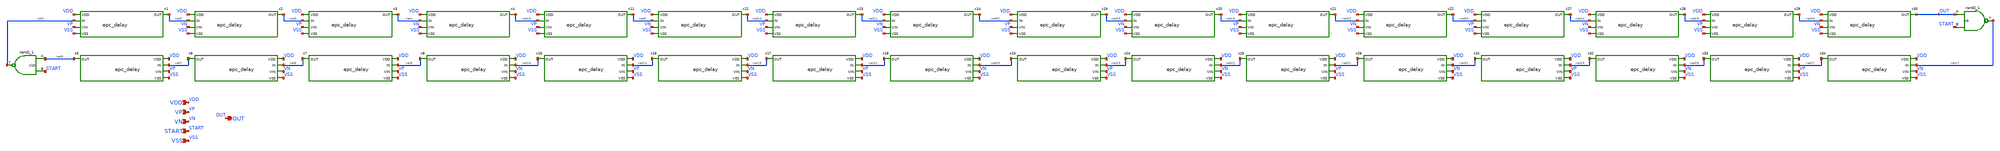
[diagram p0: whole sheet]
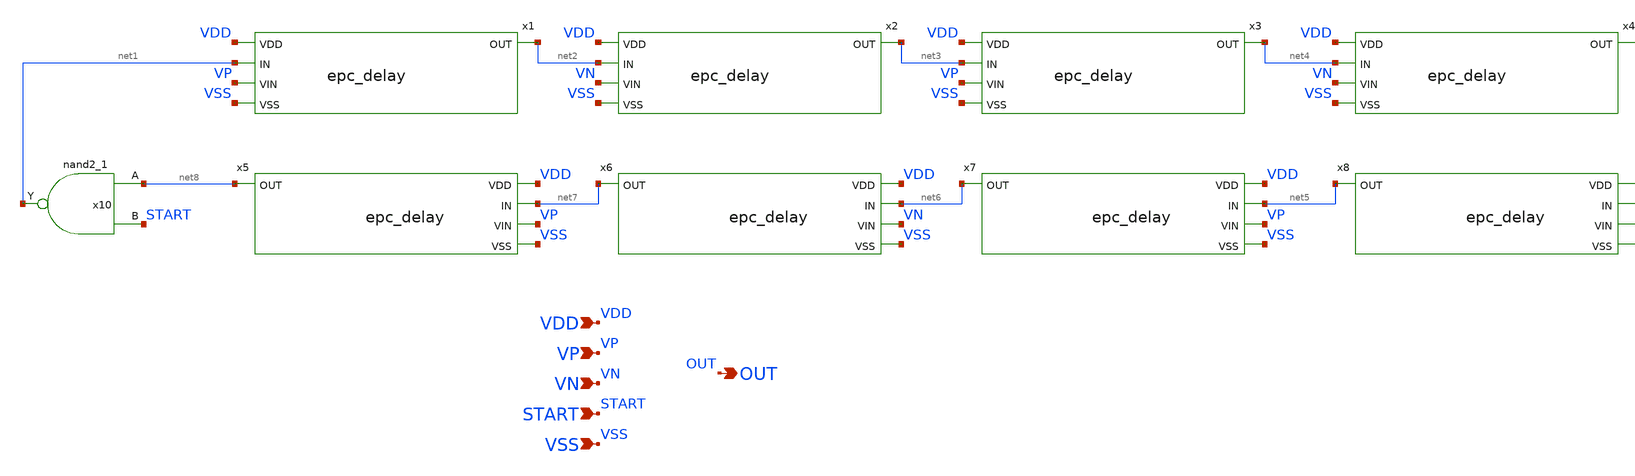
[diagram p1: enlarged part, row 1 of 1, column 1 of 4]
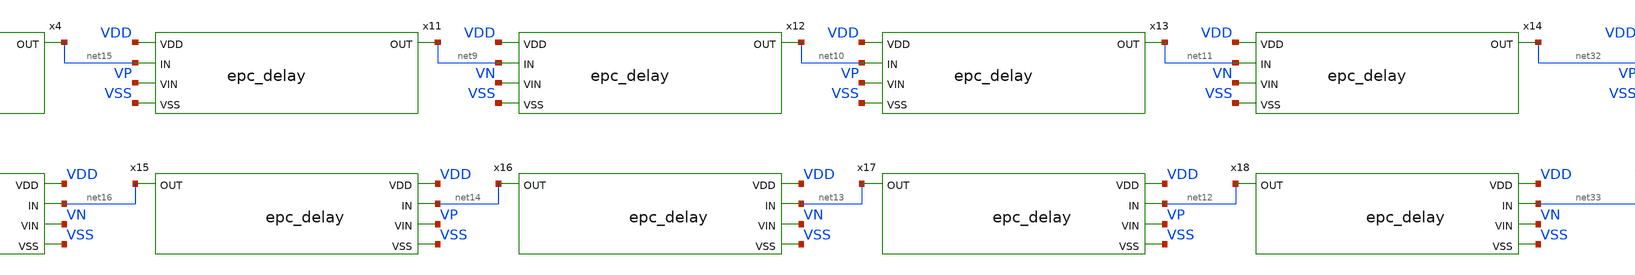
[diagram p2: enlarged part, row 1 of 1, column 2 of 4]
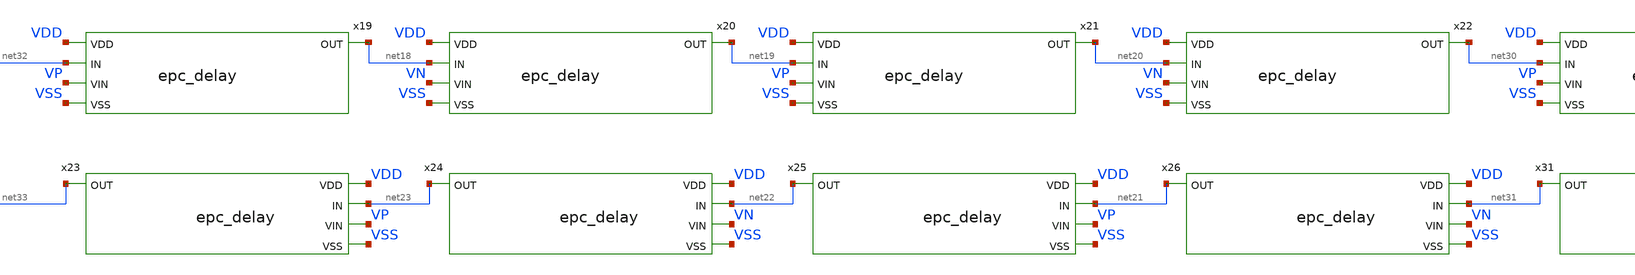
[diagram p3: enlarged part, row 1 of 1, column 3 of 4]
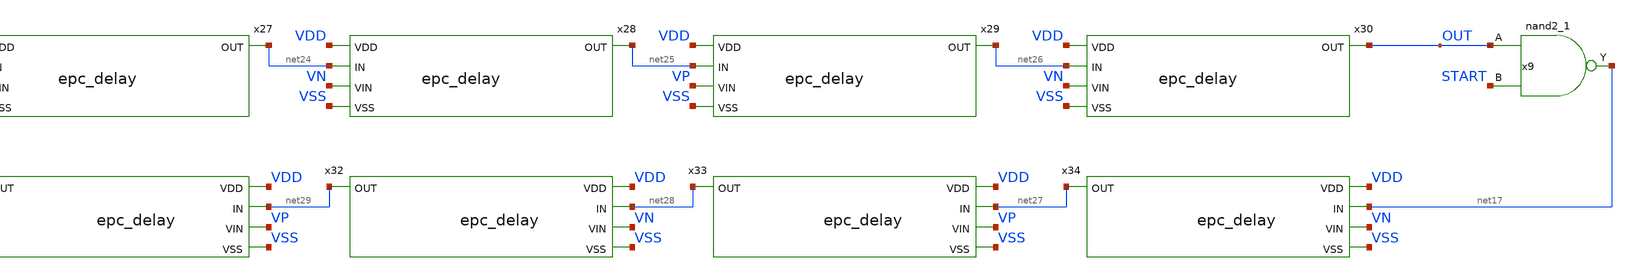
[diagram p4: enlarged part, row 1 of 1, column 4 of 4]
** sch_path: xschem/epc.sch
**.subckt epc VDD VP VN VSS OUT START
*.ipin VDD
*.ipin VP
*.ipin VN
*.ipin VSS
*.opin OUT
*.ipin START
x1 VDD net1 net2 VP VSS epc_delay
x2 VDD net2 net3 VN VSS epc_delay
x3 VDD net3 net4 VP VSS epc_delay
x4 VDD net4 net15 VN VSS epc_delay
x5 VDD net7 net8 VP VSS epc_delay
x6 VDD net6 net7 VN VSS epc_delay
x7 VDD net5 net6 VP VSS epc_delay
x8 VDD net16 net5 VN VSS epc_delay
x9 OUT START VSS VSS VDD VDD net17 sky130_fd_sc_hd__nand2_1
x10 net8 START VSS VSS VDD VDD net1 sky130_fd_sc_hd__nand2_1
x11 VDD net15 net9 VP VSS epc_delay
x12 VDD net9 net10 VN VSS epc_delay
x13 VDD net10 net11 VP VSS epc_delay
x14 VDD net11 net32 VN VSS epc_delay
x15 VDD net14 net16 VP VSS epc_delay
x16 VDD net13 net14 VN VSS epc_delay
x17 VDD net12 net13 VP VSS epc_delay
x18 VDD net33 net12 VN VSS epc_delay
x19 VDD net32 net18 VP VSS epc_delay
x20 VDD net18 net19 VN VSS epc_delay
x21 VDD net19 net20 VP VSS epc_delay
x22 VDD net20 net30 VN VSS epc_delay
x23 VDD net23 net33 VP VSS epc_delay
x24 VDD net22 net23 VN VSS epc_delay
x25 VDD net21 net22 VP VSS epc_delay
x26 VDD net31 net21 VN VSS epc_delay
x27 VDD net30 net24 VP VSS epc_delay
x28 VDD net24 net25 VN VSS epc_delay
x29 VDD net25 net26 VP VSS epc_delay
x30 VDD net26 OUT VN VSS epc_delay
x31 VDD net29 net31 VP VSS epc_delay
x32 VDD net28 net29 VN VSS epc_delay
x33 VDD net27 net28 VP VSS epc_delay
x34 VDD net17 net27 VN VSS epc_delay
**.ends
.end
